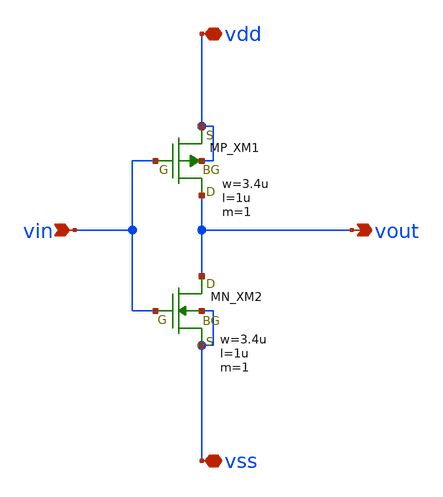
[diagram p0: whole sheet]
** sch_path: member_project/inverter/Liesegang/my_inv_gate.sch
**.subckt my_inv_gate vin vout vdd vss
*.ipin vin
*.opin vout
*.iopin vdd
*.iopin vss
XM1 vout vin vdd vdd PMOS w=3.4u l=1u as=0 ad=0 ps=0 pd=0 nrd=0 nrs=0 m=1
XM2 vout vin vss vss NMOS w=3.4u l=1u as=0 ad=0 ps=0 pd=0 nrd=0 nrs=0 m=1
**.ends
.end
